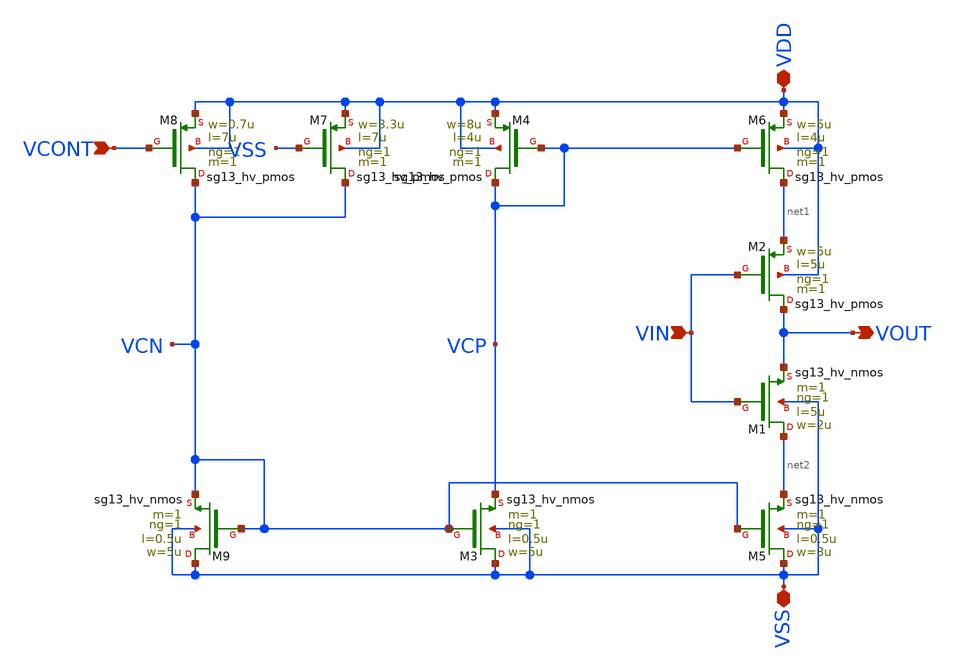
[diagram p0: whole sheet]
** sch_path: xschem/VCO/stage_vto2p1.sch
**.subckt stage_vto2p1 VIN VOUT VDD VSS VCONT
*.ipin VIN
*.opin VOUT
*.iopin VDD
*.iopin VSS
*.ipin VCONT
XM9 VSS VCN VCN VSS sg13_hv_nmos w=5u l=0.5u ng=1 m=1 mm_ok=1
XM3 VSS VCN VCP VSS sg13_hv_nmos w=5u l=0.5u ng=1 m=1 mm_ok=1
XM5 VSS VCN net2 VSS sg13_hv_nmos w=3u l=0.5u ng=1 m=1 mm_ok=1
XM8 VCN VCONT VDD VDD sg13_hv_pmos w=0.7u l=7u ng=1 m=1 mm_ok=1
XM4 VCP VCP VDD VDD sg13_hv_pmos w=8u l=4u ng=1 m=1 mm_ok=1
XM6 net1 VCP VDD VDD sg13_hv_pmos w=5u l=4u ng=1 m=1 mm_ok=1
XM2 VOUT VIN net1 VDD sg13_hv_pmos w=5u l=5u ng=1 m=1 mm_ok=1
XM1 net2 VIN VOUT VSS sg13_hv_nmos w=2u l=5u ng=1 m=1 mm_ok=1
XM7 VCN VSS VDD VDD sg13_hv_pmos w=3.3u l=7u ng=1 m=1 mm_ok=1
**.ends
.end
